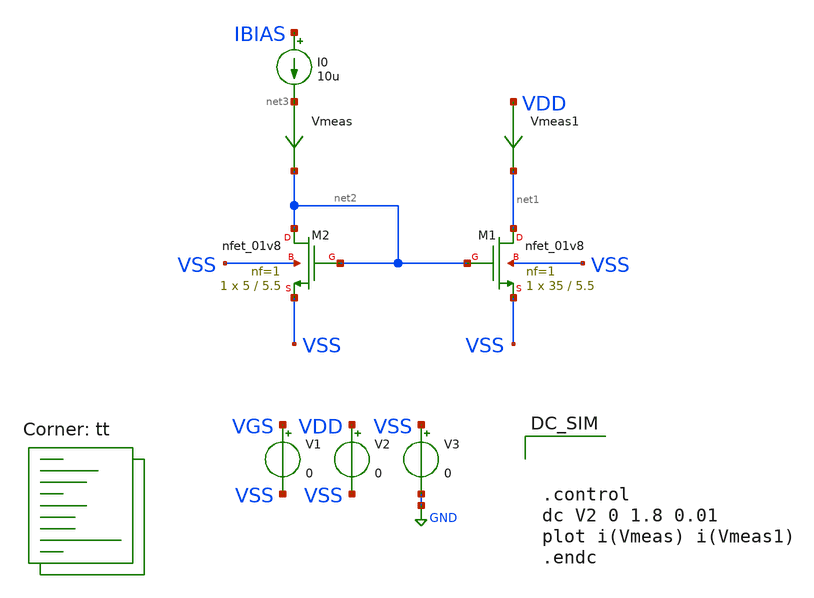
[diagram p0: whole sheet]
** sch_path: designs/libs/core_analog/p-ota/examples/fet-tb/current-mirror.sch
**.subckt current-mirror
XM1 net1 net2 VSS VSS sky130_fd_pr__nfet_01v8 L=5.5 W=35 nf=1 ad='int((nf+1)/2) * W/nf * 0.29' as='int((nf+2)/2) * W/nf * 0.29'
+ pd='2*int((nf+1)/2) * (W/nf + 0.29)' ps='2*int((nf+2)/2) * (W/nf + 0.29)' nrd='0.29 / W' nrs='0.29 / W'
+ sa=0 sb=0 sd=0 mult=1 m=1
XM2 net2 net2 VSS VSS sky130_fd_pr__nfet_01v8 L=5.5 W=5 nf=1 ad='int((nf+1)/2) * W/nf * 0.29' as='int((nf+2)/2) * W/nf * 0.29'
+ pd='2*int((nf+1)/2) * (W/nf + 0.29)' ps='2*int((nf+2)/2) * (W/nf + 0.29)' nrd='0.29 / W' nrs='0.29 / W'
+ sa=0 sb=0 sd=0 mult=1 m=1
V1 VGS VSS 0
V2 VDD VSS 0
V3 VSS GND 0
I0 IBIAS net3 10u
Vmeas net3 net2 0
.save i(vmeas)
Vmeas1 VDD net1 0
.save i(vmeas1)
**** begin user architecture code
.lib $::SKYWATER_MODELS/sky130.lib.spice tt



.control
dc V2 0 1.8 0.01
plot i(Vmeas) i(Vmeas1)
.endc

**** end user architecture code
**.ends
.GLOBAL GND
.end
